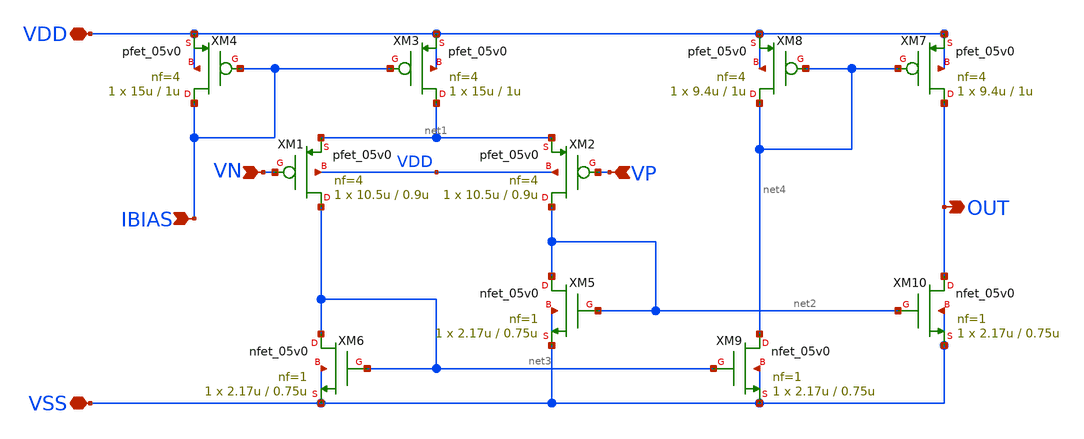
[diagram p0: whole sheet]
** sch_path: designs/symmetrical-ota/symmetrical-ota.sch
**.subckt symmetrical-ota IBIAS VN VP OUT VDD VSS
*.ipin IBIAS
*.ipin VN
*.ipin VP
*.opin OUT
*.iopin VDD
*.iopin VSS
XM1 net3 VN net1 VDD pfet_05v0 L=0.9u W=10.5u nf=4 ad='int((nf+1)/2) * W/nf * 0.18u' as='int((nf+2)/2) * W/nf * 0.18u'
+ pd='2*int((nf+1)/2) * (W/nf + 0.18u)' ps='2*int((nf+2)/2) * (W/nf + 0.18u)' nrd='0.18u / W' nrs='0.18u / W'
+ sa=0 sb=0 sd=0 m=1
XM2 net2 VP net1 VDD pfet_05v0 L=0.9u W=10.5u nf=4 ad='int((nf+1)/2) * W/nf * 0.18u' as='int((nf+2)/2) * W/nf * 0.18u'
+ pd='2*int((nf+1)/2) * (W/nf + 0.18u)' ps='2*int((nf+2)/2) * (W/nf + 0.18u)' nrd='0.18u / W' nrs='0.18u / W'
+ sa=0 sb=0 sd=0 m=1
XM3 net1 IBIAS VDD VDD pfet_05v0 L=1u W=15u nf=4 ad='int((nf+1)/2) * W/nf * 0.18u' as='int((nf+2)/2) * W/nf * 0.18u'
+ pd='2*int((nf+1)/2) * (W/nf + 0.18u)' ps='2*int((nf+2)/2) * (W/nf + 0.18u)' nrd='0.18u / W' nrs='0.18u / W'
+ sa=0 sb=0 sd=0 m=1
XM4 IBIAS IBIAS VDD VDD pfet_05v0 L=1u W=15u nf=4 ad='int((nf+1)/2) * W/nf * 0.18u' as='int((nf+2)/2) * W/nf * 0.18u'
+ pd='2*int((nf+1)/2) * (W/nf + 0.18u)' ps='2*int((nf+2)/2) * (W/nf + 0.18u)' nrd='0.18u / W' nrs='0.18u / W'
+ sa=0 sb=0 sd=0 m=1
XM5 net2 net2 VSS VSS nfet_05v0 L=0.75u W=2.17u nf=1 ad='int((nf+1)/2) * W/nf * 0.18u' as='int((nf+2)/2) * W/nf * 0.18u'
+ pd='2*int((nf+1)/2) * (W/nf + 0.18u)' ps='2*int((nf+2)/2) * (W/nf + 0.18u)' nrd='0.18u / W' nrs='0.18u / W'
+ sa=0 sb=0 sd=0 m=1
XM6 net3 net3 VSS VSS nfet_05v0 L=0.75u W=2.17u nf=1 ad='int((nf+1)/2) * W/nf * 0.18u' as='int((nf+2)/2) * W/nf * 0.18u'
+ pd='2*int((nf+1)/2) * (W/nf + 0.18u)' ps='2*int((nf+2)/2) * (W/nf + 0.18u)' nrd='0.18u / W' nrs='0.18u / W'
+ sa=0 sb=0 sd=0 m=1
XM7 OUT net4 VDD VDD pfet_05v0 L=1u W=9.4u nf=4 ad='int((nf+1)/2) * W/nf * 0.18u' as='int((nf+2)/2) * W/nf * 0.18u'
+ pd='2*int((nf+1)/2) * (W/nf + 0.18u)' ps='2*int((nf+2)/2) * (W/nf + 0.18u)' nrd='0.18u / W' nrs='0.18u / W'
+ sa=0 sb=0 sd=0 m=1
XM8 net4 net4 VDD VDD pfet_05v0 L=1u W=9.4u nf=4 ad='int((nf+1)/2) * W/nf * 0.18u' as='int((nf+2)/2) * W/nf * 0.18u'
+ pd='2*int((nf+1)/2) * (W/nf + 0.18u)' ps='2*int((nf+2)/2) * (W/nf + 0.18u)' nrd='0.18u / W' nrs='0.18u / W'
+ sa=0 sb=0 sd=0 m=1
XM9 net4 net3 VSS VSS nfet_05v0 L=0.75u W=2.17u nf=1 ad='int((nf+1)/2) * W/nf * 0.18u' as='int((nf+2)/2) * W/nf * 0.18u'
+ pd='2*int((nf+1)/2) * (W/nf + 0.18u)' ps='2*int((nf+2)/2) * (W/nf + 0.18u)' nrd='0.18u / W' nrs='0.18u / W'
+ sa=0 sb=0 sd=0 m=1
XM10 OUT net2 VSS VSS nfet_05v0 L=0.75u W=2.17u nf=1 ad='int((nf+1)/2) * W/nf * 0.18u' as='int((nf+2)/2) * W/nf * 0.18u'
+ pd='2*int((nf+1)/2) * (W/nf + 0.18u)' ps='2*int((nf+2)/2) * (W/nf + 0.18u)' nrd='0.18u / W' nrs='0.18u / W'
+ sa=0 sb=0 sd=0 m=1
**.ends
.end
